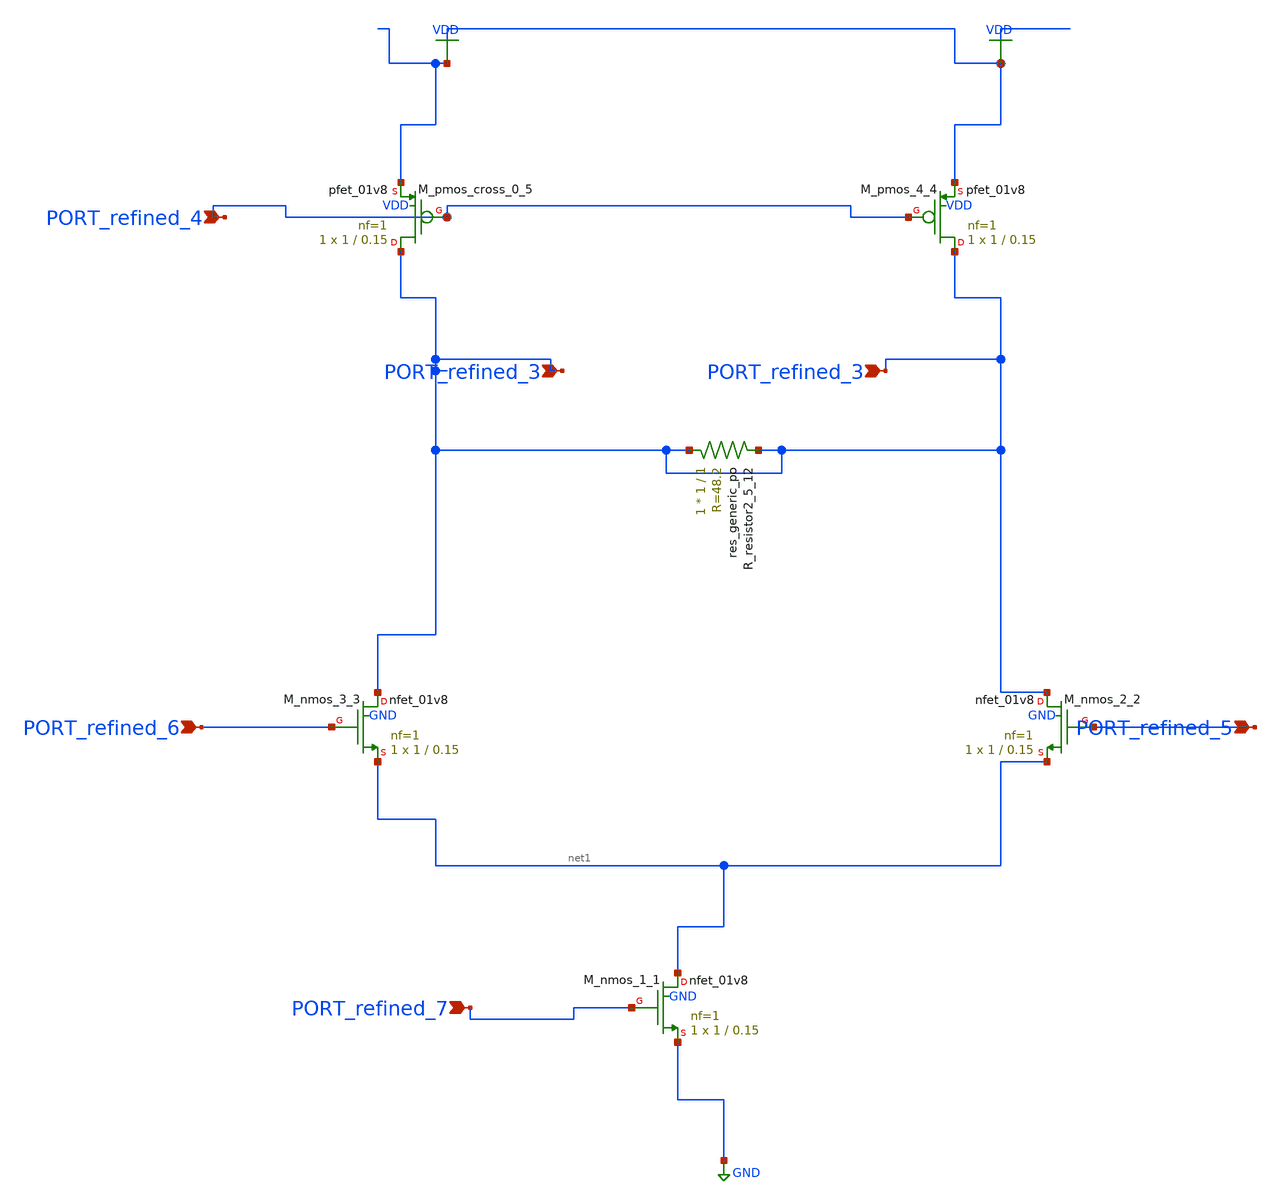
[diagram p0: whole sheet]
** sch_path: schematics/AMSNet/239.sch
**.subckt 239 PORT_refined_5 PORT_refined_3 PORT_refined_3 PORT_refined_6 PORT_refined_7
*+ PORT_refined_4
*.ipin PORT_refined_5
*.ipin PORT_refined_3
*.ipin PORT_refined_3
*.ipin PORT_refined_6
*.ipin PORT_refined_7
*.ipin PORT_refined_4
XM_nmos_1_1 net1 PORT_refined_7 GND GND sky130_fd_pr__nfet_01v8 L=0.15 W=1 nf=1 ad='int((1 + 1)/2) * 1 / 1 * 0.29'
+ as='int((1 + 2)/2) * 1 / 1 * 0.29' pd='2*int((1 + 1)/2) * (1 / 1 + 0.29)' ps='2*int((1 + 2)/2) * (1 / 1 + 0.29)'
+ nrd='0.29 / 1 ' nrs='0.29 / 1 ' sa=0 sb=0 sd=0 mult=1 m=1
XM_nmos_2_2 PORT_refined_3 PORT_refined_5 net1 GND sky130_fd_pr__nfet_01v8 L=0.15 W=1 nf=1 ad='int((1 + 1)/2) * 1 / 1 * 0.29'
+ as='int((1 + 2)/2) * 1 / 1 * 0.29' pd='2*int((1 + 1)/2) * (1 / 1 + 0.29)' ps='2*int((1 + 2)/2) * (1 / 1 + 0.29)'
+ nrd='0.29 / 1 ' nrs='0.29 / 1 ' sa=0 sb=0 sd=0 mult=1 m=1
XM_nmos_3_3 PORT_refined_3 PORT_refined_6 net1 GND sky130_fd_pr__nfet_01v8 L=0.15 W=1 nf=1 ad='int((1 + 1)/2) * 1 / 1 * 0.29'
+ as='int((1 + 2)/2) * 1 / 1 * 0.29' pd='2*int((1 + 1)/2) * (1 / 1 + 0.29)' ps='2*int((1 + 2)/2) * (1 / 1 + 0.29)'
+ nrd='0.29 / 1 ' nrs='0.29 / 1 ' sa=0 sb=0 sd=0 mult=1 m=1
XM_pmos_4_4 PORT_refined_3 PORT_refined_4 VDD VDD sky130_fd_pr__pfet_01v8 L=0.15 W=1 nf=1 ad='int((1 + 1)/2) * 1 / 1 * 0.29'
+ as='int((1 + 2)/2) * 1 / 1 * 0.29' pd='2*int((1 + 1)/2) * (1 / 1 + 0.29)' ps='2*int((1 + 2)/2) * (1 / 1 + 0.29)'
+ nrd='0.29 / 1 ' nrs='0.29 / 1 ' sa=0 sb=0 sd=0 mult=1 m=1
XM_pmos_cross_0_5 PORT_refined_3 PORT_refined_4 VDD VDD sky130_fd_pr__pfet_01v8 L=0.15 W=1 nf=1 ad='int((1 + 1)/2) * 1 / 1 * 0.29'
+ as='int((1 + 2)/2) * 1 / 1 * 0.29' pd='2*int((1 + 1)/2) * (1 / 1 + 0.29)' ps='2*int((1 + 2)/2) * (1 / 1 + 0.29)'
+ nrd='0.29 / 1 ' nrs='0.29 / 1 ' sa=0 sb=0 sd=0 mult=1 m=1
XR_resistor2_5_12 PORT_refined_3 PORT_refined_3 sky130_fd_pr__res_generic_po W=1 L=1 m=1
**.ends
.GLOBAL GND
.GLOBAL VDD
.end
